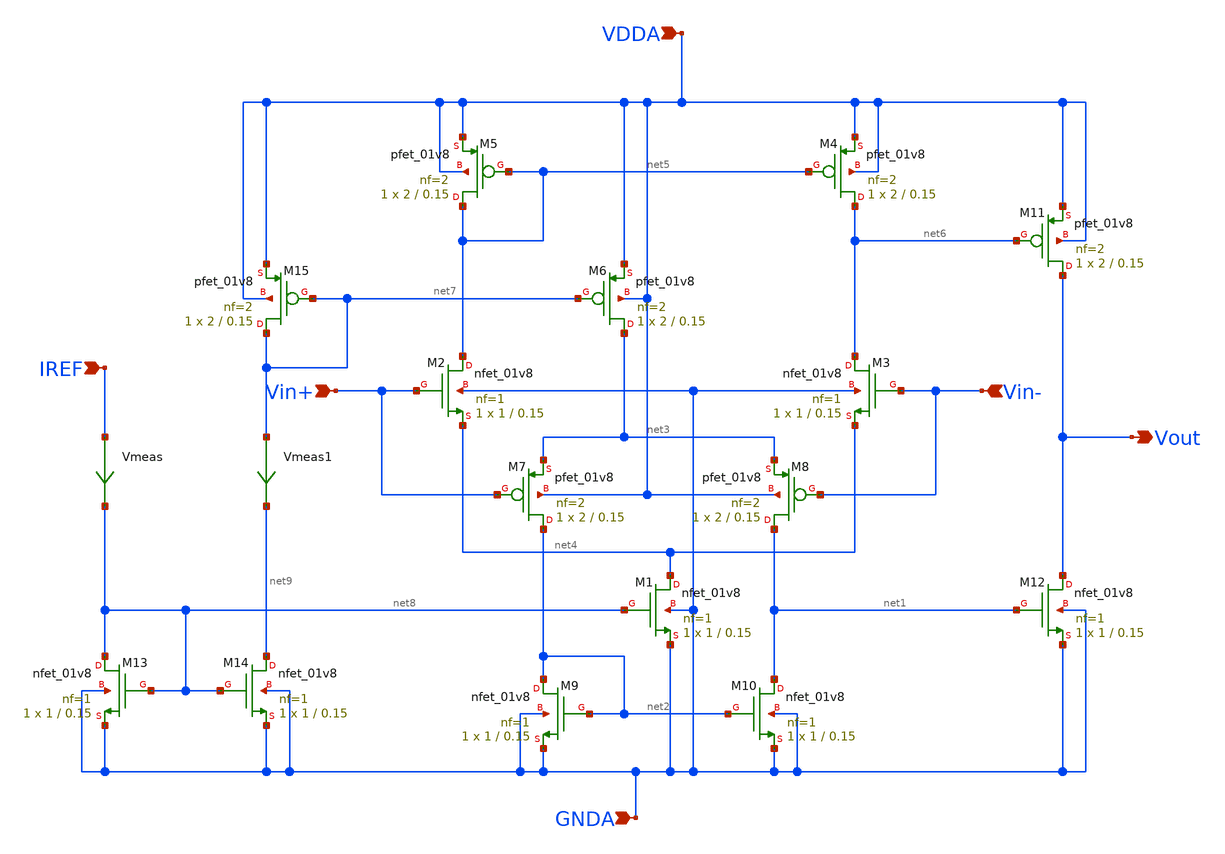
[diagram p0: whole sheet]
** sch_path: projects/pll/charge_pump/xschem_ngspice/rail_to_rail_opamp.sch
**.subckt rail_to_rail_opamp IREF Vout Vin+ Vin- VDDA GNDA
*.ipin IREF
*.opin Vout
*.ipin Vin+
*.ipin Vin-
*.ipin VDDA
*.ipin GNDA
XM2 net5 Vin+ net4 GNDA sky130_fd_pr__nfet_01v8 L=0.15 W=1 nf=1 ad='int((nf+1)/2) * W/nf * 0.29' as='int((nf+2)/2) * W/nf * 0.29'
+ pd='2*int((nf+1)/2) * (W/nf + 0.29)' ps='2*int((nf+2)/2) * (W/nf + 0.29)' nrd='0.29 / W' nrs='0.29 / W'
+ sa=0 sb=0 sd=0 mult=1 m=1
XM3 net6 Vin- net4 GNDA sky130_fd_pr__nfet_01v8 L=0.15 W=1 nf=1 ad='int((nf+1)/2) * W/nf * 0.29' as='int((nf+2)/2) * W/nf * 0.29'
+ pd='2*int((nf+1)/2) * (W/nf + 0.29)' ps='2*int((nf+2)/2) * (W/nf + 0.29)' nrd='0.29 / W' nrs='0.29 / W'
+ sa=0 sb=0 sd=0 mult=1 m=1
XM5 net5 net5 VDDA VDDA sky130_fd_pr__pfet_01v8 L=0.15 W=2 nf=2 ad='int((nf+1)/2) * W/nf * 0.29' as='int((nf+2)/2) * W/nf * 0.29'
+ pd='2*int((nf+1)/2) * (W/nf + 0.29)' ps='2*int((nf+2)/2) * (W/nf + 0.29)' nrd='0.29 / W' nrs='0.29 / W'
+ sa=0 sb=0 sd=0 mult=1 m=1
XM4 net6 net5 VDDA VDDA sky130_fd_pr__pfet_01v8 L=0.15 W=2 nf=2 ad='int((nf+1)/2) * W/nf * 0.29' as='int((nf+2)/2) * W/nf * 0.29'
+ pd='2*int((nf+1)/2) * (W/nf + 0.29)' ps='2*int((nf+2)/2) * (W/nf + 0.29)' nrd='0.29 / W' nrs='0.29 / W'
+ sa=0 sb=0 sd=0 mult=1 m=1
XM6 net3 net7 VDDA VDDA sky130_fd_pr__pfet_01v8 L=0.15 W=2 nf=2 ad='int((nf+1)/2) * W/nf * 0.29' as='int((nf+2)/2) * W/nf * 0.29'
+ pd='2*int((nf+1)/2) * (W/nf + 0.29)' ps='2*int((nf+2)/2) * (W/nf + 0.29)' nrd='0.29 / W' nrs='0.29 / W'
+ sa=0 sb=0 sd=0 mult=1 m=1
XM7 net2 Vin+ net3 VDDA sky130_fd_pr__pfet_01v8 L=0.15 W=2 nf=2 ad='int((nf+1)/2) * W/nf * 0.29' as='int((nf+2)/2) * W/nf * 0.29'
+ pd='2*int((nf+1)/2) * (W/nf + 0.29)' ps='2*int((nf+2)/2) * (W/nf + 0.29)' nrd='0.29 / W' nrs='0.29 / W'
+ sa=0 sb=0 sd=0 mult=1 m=1
XM8 net1 Vin- net3 VDDA sky130_fd_pr__pfet_01v8 L=0.15 W=2 nf=2 ad='int((nf+1)/2) * W/nf * 0.29' as='int((nf+2)/2) * W/nf * 0.29'
+ pd='2*int((nf+1)/2) * (W/nf + 0.29)' ps='2*int((nf+2)/2) * (W/nf + 0.29)' nrd='0.29 / W' nrs='0.29 / W'
+ sa=0 sb=0 sd=0 mult=1 m=1
XM9 net2 net2 GNDA GNDA sky130_fd_pr__nfet_01v8 L=0.15 W=1 nf=1 ad='int((nf+1)/2) * W/nf * 0.29' as='int((nf+2)/2) * W/nf * 0.29'
+ pd='2*int((nf+1)/2) * (W/nf + 0.29)' ps='2*int((nf+2)/2) * (W/nf + 0.29)' nrd='0.29 / W' nrs='0.29 / W'
+ sa=0 sb=0 sd=0 mult=1 m=1
XM10 net1 net2 GNDA GNDA sky130_fd_pr__nfet_01v8 L=0.15 W=1 nf=1 ad='int((nf+1)/2) * W/nf * 0.29' as='int((nf+2)/2) * W/nf * 0.29'
+ pd='2*int((nf+1)/2) * (W/nf + 0.29)' ps='2*int((nf+2)/2) * (W/nf + 0.29)' nrd='0.29 / W' nrs='0.29 / W'
+ sa=0 sb=0 sd=0 mult=1 m=1
XM1 net4 net8 GNDA GNDA sky130_fd_pr__nfet_01v8 L=0.15 W=1 nf=1 ad='int((nf+1)/2) * W/nf * 0.29' as='int((nf+2)/2) * W/nf * 0.29'
+ pd='2*int((nf+1)/2) * (W/nf + 0.29)' ps='2*int((nf+2)/2) * (W/nf + 0.29)' nrd='0.29 / W' nrs='0.29 / W'
+ sa=0 sb=0 sd=0 mult=1 m=1
XM11 Vout net6 VDDA VDDA sky130_fd_pr__pfet_01v8 L=0.15 W=2 nf=2 ad='int((nf+1)/2) * W/nf * 0.29' as='int((nf+2)/2) * W/nf * 0.29'
+ pd='2*int((nf+1)/2) * (W/nf + 0.29)' ps='2*int((nf+2)/2) * (W/nf + 0.29)' nrd='0.29 / W' nrs='0.29 / W'
+ sa=0 sb=0 sd=0 mult=1 m=1
XM12 Vout net1 GNDA GNDA sky130_fd_pr__nfet_01v8 L=0.15 W=1 nf=1 ad='int((nf+1)/2) * W/nf * 0.29' as='int((nf+2)/2) * W/nf * 0.29'
+ pd='2*int((nf+1)/2) * (W/nf + 0.29)' ps='2*int((nf+2)/2) * (W/nf + 0.29)' nrd='0.29 / W' nrs='0.29 / W'
+ sa=0 sb=0 sd=0 mult=1 m=1
XM13 net8 net8 GNDA GNDA sky130_fd_pr__nfet_01v8 L=0.15 W=1 nf=1 ad='int((nf+1)/2) * W/nf * 0.29' as='int((nf+2)/2) * W/nf * 0.29'
+ pd='2*int((nf+1)/2) * (W/nf + 0.29)' ps='2*int((nf+2)/2) * (W/nf + 0.29)' nrd='0.29 / W' nrs='0.29 / W'
+ sa=0 sb=0 sd=0 mult=1 m=1
XM14 net9 net8 GNDA GNDA sky130_fd_pr__nfet_01v8 L=0.15 W=1 nf=1 ad='int((nf+1)/2) * W/nf * 0.29' as='int((nf+2)/2) * W/nf * 0.29'
+ pd='2*int((nf+1)/2) * (W/nf + 0.29)' ps='2*int((nf+2)/2) * (W/nf + 0.29)' nrd='0.29 / W' nrs='0.29 / W'
+ sa=0 sb=0 sd=0 mult=1 m=1
XM15 net7 net7 VDDA VDDA sky130_fd_pr__pfet_01v8 L=0.15 W=2 nf=2 ad='int((nf+1)/2) * W/nf * 0.29' as='int((nf+2)/2) * W/nf * 0.29'
+ pd='2*int((nf+1)/2) * (W/nf + 0.29)' ps='2*int((nf+2)/2) * (W/nf + 0.29)' nrd='0.29 / W' nrs='0.29 / W'
+ sa=0 sb=0 sd=0 mult=1 m=1
Vmeas IREF net8 0
.save i(vmeas)
Vmeas1 net7 net9 0
.save i(vmeas1)
**.ends
.end
